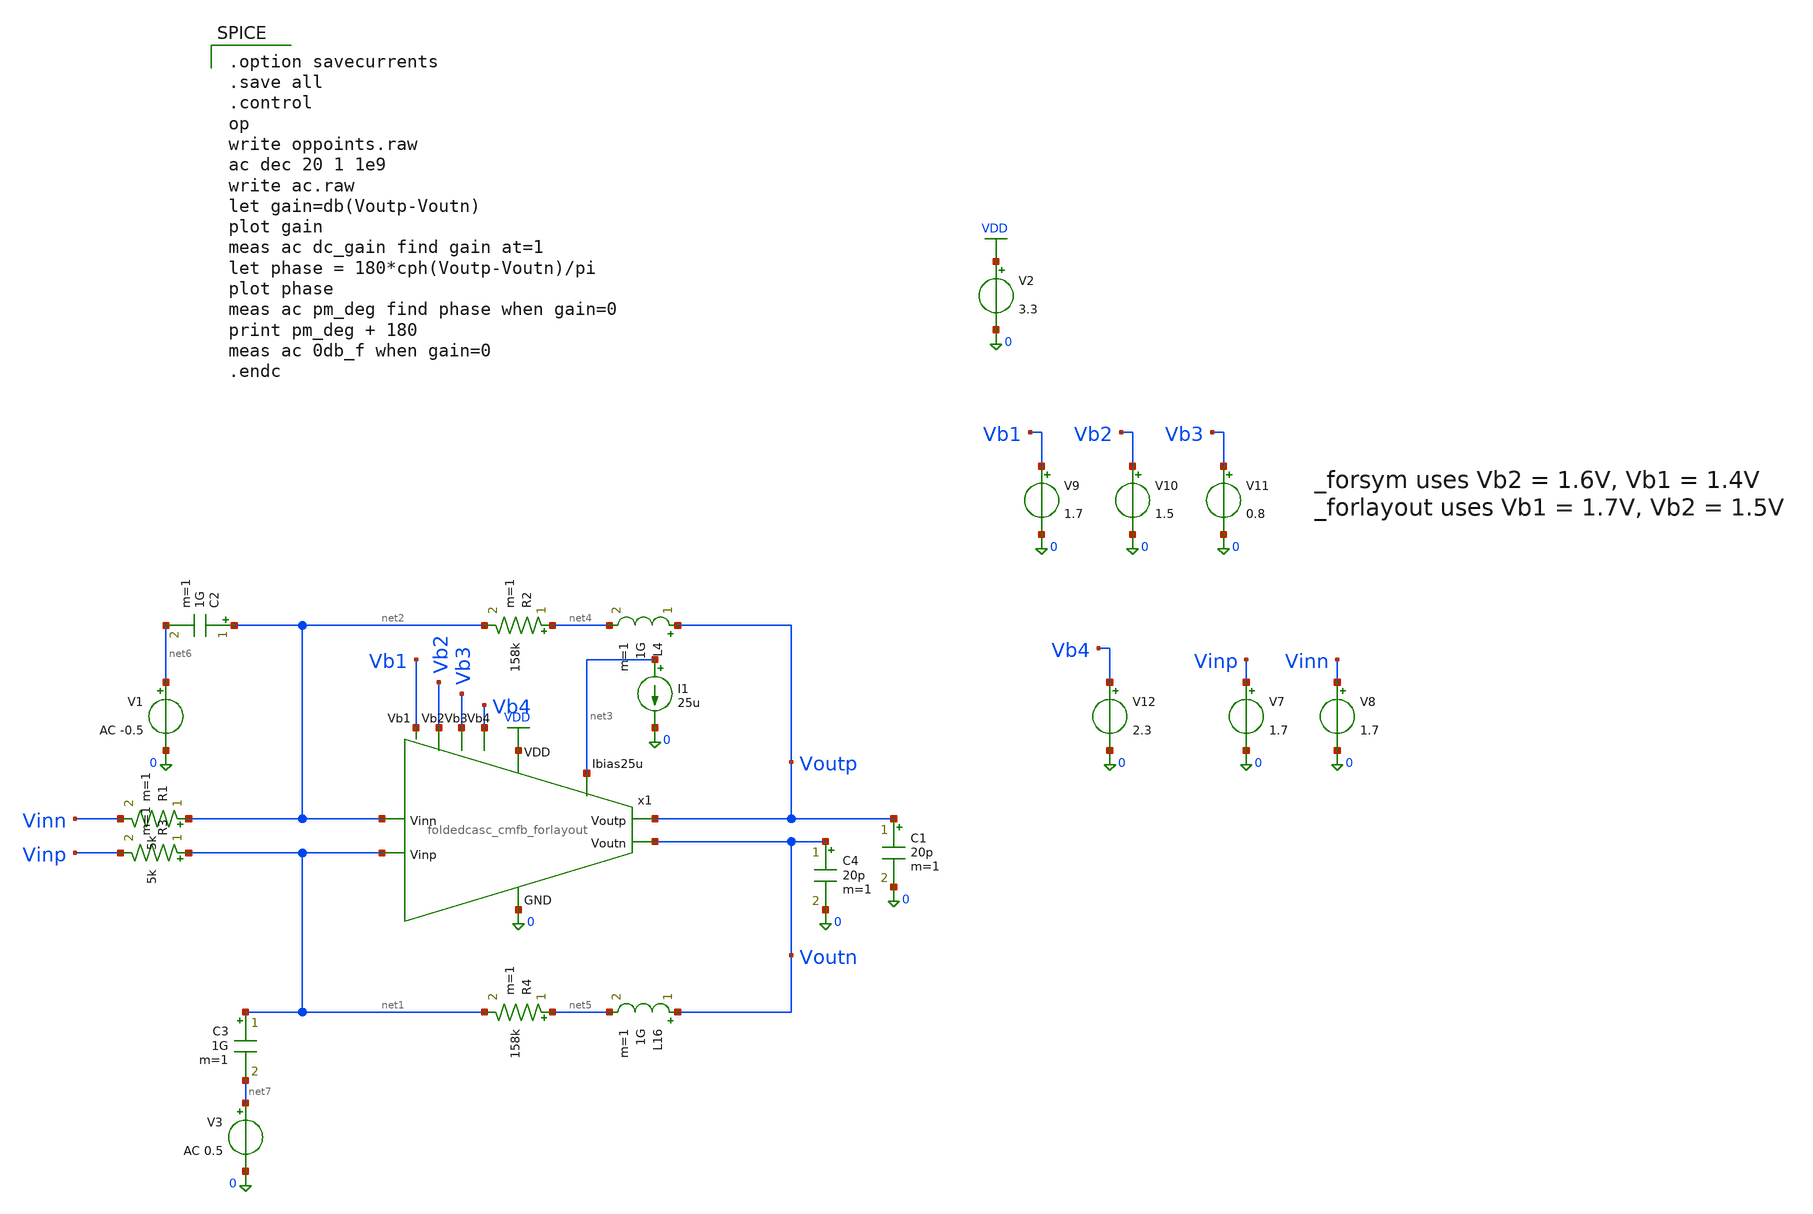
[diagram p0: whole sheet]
** sch_path: jz_fda2/xschem/fda2_loopgain_tb.sch
**.subckt fda2_loopgain_tb
C4 Voutn 0 20p m=1
C1 Voutp 0 20p m=1
I1 net3 0 25u
V2 VDD 0 3.3
V9 Vb1 0 1.7
V10 Vb2 0 1.5
V11 Vb3 0 0.8
V12 Vb4 0 2.3
V7 Vinp 0 1.7
V8 Vinn 0 1.7
R3 net1 Vinp 5k m=1
R1 net2 Vinn 5k m=1
R2 net4 net2 158k m=1
R4 net5 net1 158k m=1
L4 Voutp net4 1G m=1
V1 net6 0 AC -0.5
V3 net7 0 AC 0.5
L16 Voutn net5 1G m=1
C2 net2 net6 1G m=1
C3 net1 net7 1G m=1
x1 VDD Vb2 Voutp Voutn Vb1 net3 net2 0 net1 Vb3 Vb4 foldedcasc_cmfb_forlayout
**** begin user architecture code

.include $::180MCU_MODELS/design.ngspice
.lib $::180MCU_MODELS/sm141064.ngspice typical
.lib $::180MCU_MODELS/smbb000149.ngspice typical


.option savecurrents
.save all
.control
op
write oppoints.raw
ac dec 20 1 1e9
write ac.raw
let gain=db(Voutp-Voutn)
plot gain
meas ac dc_gain find gain at=1
let phase = 180*cph(Voutp-Voutn)/pi
plot phase
meas ac pm_deg find phase when gain=0
print pm_deg + 180
meas ac 0db_f when gain=0
.endc

**** end user architecture code
**.ends

* expanding   symbol:  chipathon-2026-ppg/jz_fda2/xschem/foldedcasc_cmfb_forlayout.sym # of pins=11
** sym_path: jz_fda2/xschem/foldedcasc_cmfb_forlayout.sym
** sch_path: jz_fda2/xschem/foldedcasc_cmfb_forlayout.sch
.subckt foldedcasc_cmfb_forlayout VDD Vb2 Voutp Voutn Vb1 Ibias25u Vinn GND Vinp Vb3 Vb4
*.ipin VDD
*.opin Voutp
*.ipin Vinn
*.ipin Ibias25u
*.ipin GND
*.ipin Vinp
*.opin Voutn
*.ipin Vb4
*.ipin Vb1
*.ipin Vb2
*.ipin Vb3
XM5 net1 Vb3 GND GND nfet_03v3 L=0.28u W=13u nf=4 ad='int((nf+1)/2) * W/nf * 0.18u' as='int((nf+2)/2) * W/nf * 0.18u'
+ pd='2*int((nf+1)/2) * (W/nf + 0.18u)' ps='2*int((nf+2)/2) * (W/nf + 0.18u)' nrd='0.18u / W' nrs='0.18u / W'
+ sa=0 sb=0 sd=0 m=1
XM6 Voutn Vb2 net2 GND nfet_03v3 L=0.28u W=6.6u nf=2 ad='int((nf+1)/2) * W/nf * 0.18u' as='int((nf+2)/2) * W/nf * 0.18u'
+ pd='2*int((nf+1)/2) * (W/nf + 0.18u)' ps='2*int((nf+2)/2) * (W/nf + 0.18u)' nrd='0.18u / W' nrs='0.18u / W'
+ sa=0 sb=0 sd=0 m=1
XM7 Voutp Vb2 net1 GND nfet_03v3 L=0.28u W=6.6u nf=2 ad='int((nf+1)/2) * W/nf * 0.18u' as='int((nf+2)/2) * W/nf * 0.18u'
+ pd='2*int((nf+1)/2) * (W/nf + 0.18u)' ps='2*int((nf+2)/2) * (W/nf + 0.18u)' nrd='0.18u / W' nrs='0.18u / W'
+ sa=0 sb=0 sd=0 m=1
XM8 Voutn Vb1 net3 VDD pfet_03v3 L=0.28u W=19u nf=5 ad='int((nf+1)/2) * W/nf * 0.18u' as='int((nf+2)/2) * W/nf * 0.18u'
+ pd='2*int((nf+1)/2) * (W/nf + 0.18u)' ps='2*int((nf+2)/2) * (W/nf + 0.18u)' nrd='0.18u / W' nrs='0.18u / W'
+ sa=0 sb=0 sd=0 m=1
XM9 Voutp Vb1 net4 VDD pfet_03v3 L=0.28u W=19u nf=5 ad='int((nf+1)/2) * W/nf * 0.18u' as='int((nf+2)/2) * W/nf * 0.18u'
+ pd='2*int((nf+1)/2) * (W/nf + 0.18u)' ps='2*int((nf+2)/2) * (W/nf + 0.18u)' nrd='0.18u / W' nrs='0.18u / W'
+ sa=0 sb=0 sd=0 m=1
XM10 net3 Vb4 VDD VDD pfet_03v3 L=0.28u W=16.2u nf=4 ad='int((nf+1)/2) * W/nf * 0.18u' as='int((nf+2)/2) * W/nf * 0.18u'
+ pd='2*int((nf+1)/2) * (W/nf + 0.18u)' ps='2*int((nf+2)/2) * (W/nf + 0.18u)' nrd='0.18u / W' nrs='0.18u / W'
+ sa=0 sb=0 sd=0 m=1
XM11 net4 Vb4 VDD VDD pfet_03v3 L=0.28u W=16.2u nf=4 ad='int((nf+1)/2) * W/nf * 0.18u' as='int((nf+2)/2) * W/nf * 0.18u'
+ pd='2*int((nf+1)/2) * (W/nf + 0.18u)' ps='2*int((nf+2)/2) * (W/nf + 0.18u)' nrd='0.18u / W' nrs='0.18u / W'
+ sa=0 sb=0 sd=0 m=1
XM1 net1 Vinn net5 VDD pfet_03v3 L=0.28u W=3.45u nf=1 ad='int((nf+1)/2) * W/nf * 0.18u' as='int((nf+2)/2) * W/nf * 0.18u'
+ pd='2*int((nf+1)/2) * (W/nf + 0.18u)' ps='2*int((nf+2)/2) * (W/nf + 0.18u)' nrd='0.18u / W' nrs='0.18u / W'
+ sa=0 sb=0 sd=0 m=1
XM2 net2 Vinp net5 VDD pfet_03v3 L=0.28u W=3.45u nf=1 ad='int((nf+1)/2) * W/nf * 0.18u' as='int((nf+2)/2) * W/nf * 0.18u'
+ pd='2*int((nf+1)/2) * (W/nf + 0.18u)' ps='2*int((nf+2)/2) * (W/nf + 0.18u)' nrd='0.18u / W' nrs='0.18u / W'
+ sa=0 sb=0 sd=0 m=1
XM3 net5 Ibias25u net6 VDD pfet_03v3 L=0.28u W=4.9u nf=2 ad='int((nf+1)/2) * W/nf * 0.18u' as='int((nf+2)/2) * W/nf * 0.18u'
+ pd='2*int((nf+1)/2) * (W/nf + 0.18u)' ps='2*int((nf+2)/2) * (W/nf + 0.18u)' nrd='0.18u / W' nrs='0.18u / W'
+ sa=0 sb=0 sd=0 m=1
XM12 Ibias25u Ibias25u VDD VDD pfet_03v3 L=0.28u W=2.27u nf=1 ad='int((nf+1)/2) * W/nf * 0.18u' as='int((nf+2)/2) * W/nf * 0.18u'
+ pd='2*int((nf+1)/2) * (W/nf + 0.18u)' ps='2*int((nf+2)/2) * (W/nf + 0.18u)' nrd='0.18u / W' nrs='0.18u / W'
+ sa=0 sb=0 sd=0 m=1
XM13 net6 Voutp VDD VDD pfet_03v3 L=0.28u W=30u nf=3 ad='int((nf+1)/2) * W/nf * 0.18u' as='int((nf+2)/2) * W/nf * 0.18u'
+ pd='2*int((nf+1)/2) * (W/nf + 0.18u)' ps='2*int((nf+2)/2) * (W/nf + 0.18u)' nrd='0.18u / W' nrs='0.18u / W'
+ sa=0 sb=0 sd=0 m=1
XM14 net6 Voutn VDD VDD pfet_03v3 L=0.28u W=30u nf=3 ad='int((nf+1)/2) * W/nf * 0.18u' as='int((nf+2)/2) * W/nf * 0.18u'
+ pd='2*int((nf+1)/2) * (W/nf + 0.18u)' ps='2*int((nf+2)/2) * (W/nf + 0.18u)' nrd='0.18u / W' nrs='0.18u / W'
+ sa=0 sb=0 sd=0 m=1
XM4 net2 Vb3 GND GND nfet_03v3 L=0.28u W=13u nf=4 ad='int((nf+1)/2) * W/nf * 0.18u' as='int((nf+2)/2) * W/nf * 0.18u'
+ pd='2*int((nf+1)/2) * (W/nf + 0.18u)' ps='2*int((nf+2)/2) * (W/nf + 0.18u)' nrd='0.18u / W' nrs='0.18u / W'
+ sa=0 sb=0 sd=0 m=1
.ends

.GLOBAL VDD
.end
